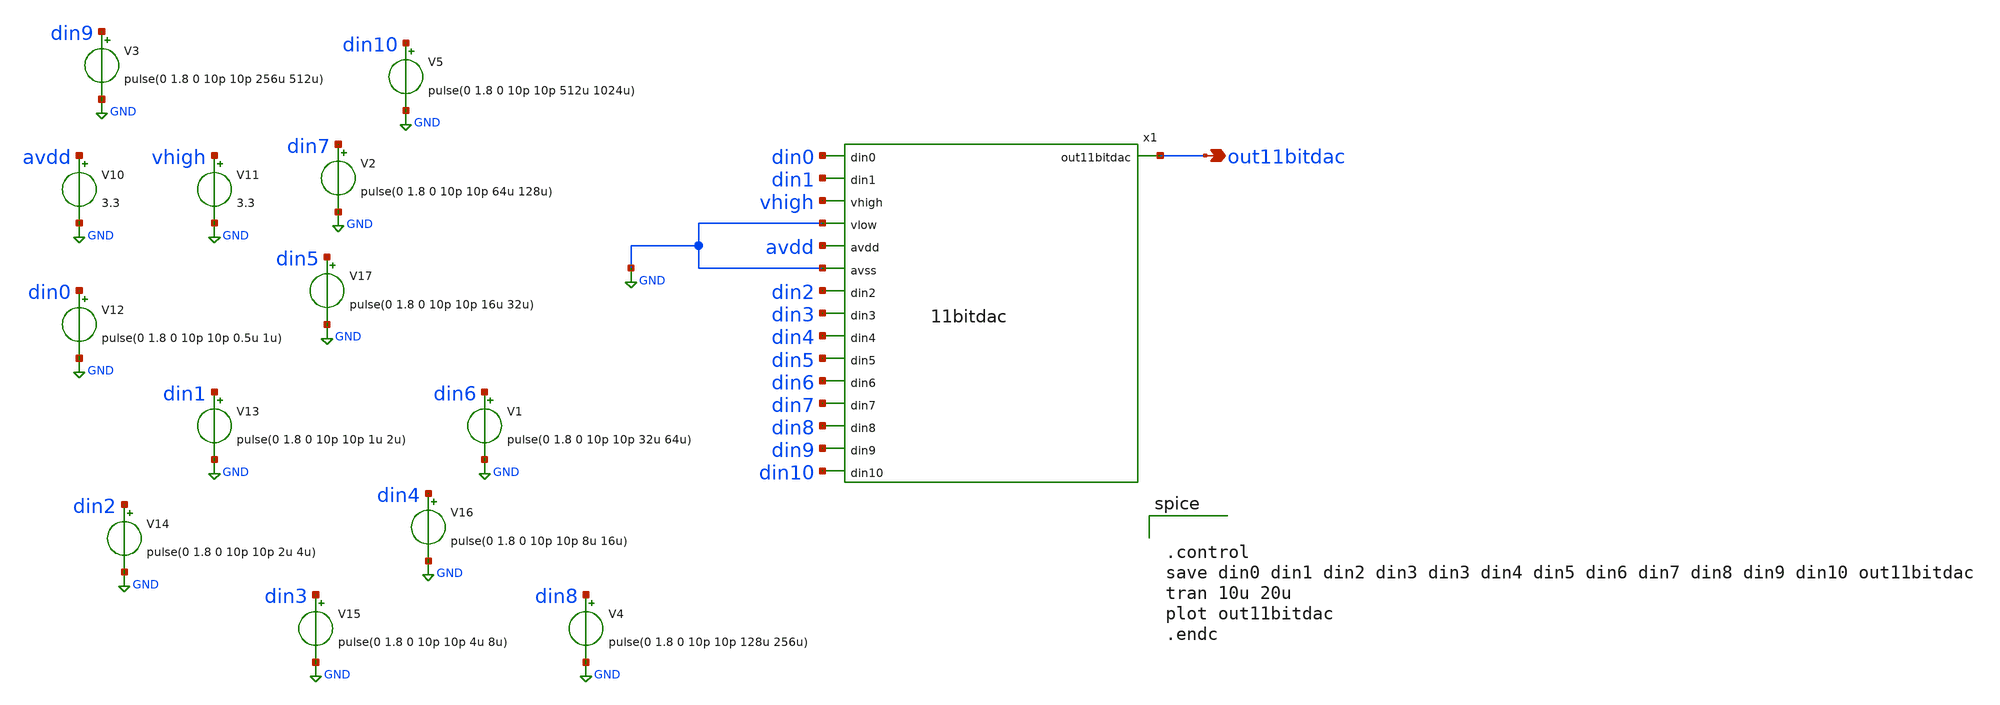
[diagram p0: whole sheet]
** sch_path: xschem/tb_11bitdac.sch
**.subckt tb_11bitdac out11bitdac
*.opin out11bitdac
x1 out11bitdac din0 din1 vhigh GND avdd GND din2 din3 din4 din5 din6 din7 din8 din9 din10 11bitdac
V10 avdd GND 3.3
V11 vhigh GND 3.3
V12 din0 GND pulse(0 1.8 0 10p 10p 0.5u 1u)
V13 din1 GND pulse(0 1.8 0 10p 10p 1u 2u)
V14 din2 GND pulse(0 1.8 0 10p 10p 2u 4u)
V15 din3 GND pulse(0 1.8 0 10p 10p 4u 8u)
V16 din4 GND pulse(0 1.8 0 10p 10p 8u 16u)
V17 din5 GND pulse(0 1.8 0 10p 10p 16u 32u)
V1 din6 GND pulse(0 1.8 0 10p 10p 32u 64u)
V2 din7 GND pulse(0 1.8 0 10p 10p 64u 128u)
V3 din9 GND pulse(0 1.8 0 10p 10p 256u 512u)
V4 din8 GND pulse(0 1.8 0 10p 10p 128u 256u)
V5 din10 GND pulse(0 1.8 0 10p 10p 512u 1024u)
**** begin user architecture code

** opencircuitdesign pdks install
.lib $::SKYWATER_MODELS/sky130.lib.spice tt




.control
save din0 din1 din2 din3 din3 din4 din5 din6 din7 din8 din9 din10 out11bitdac
tran 10u 20u
plot out11bitdac
.endc

**** end user architecture code
**.ends
.GLOBAL GND
.end
